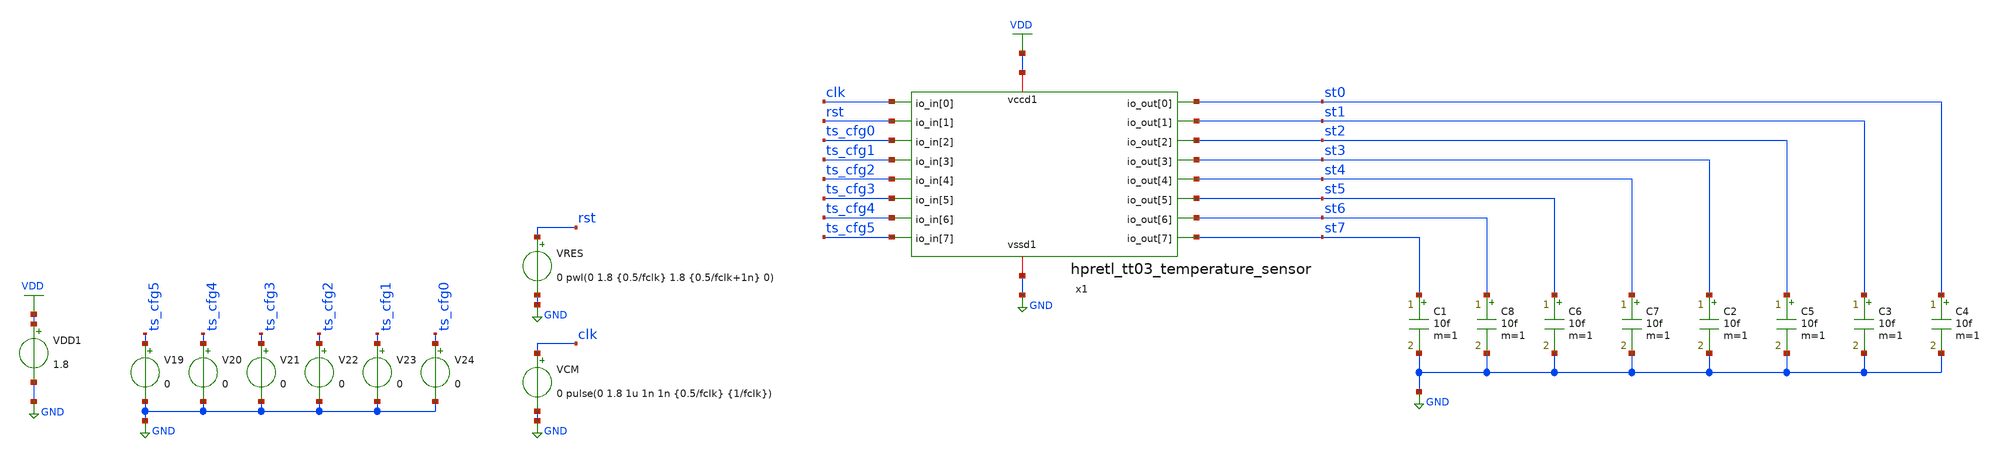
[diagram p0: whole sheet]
** sch_path: sim/tb_tempsens.sch
**.subckt tb_tempsens
VDD1 VDD GND 1.8
V19 ts_cfg5 GND 0
V20 ts_cfg4 GND 0
V21 ts_cfg3 GND 0
V22 ts_cfg2 GND 0
V23 ts_cfg1 GND 0
V24 ts_cfg0 GND 0
VCM clk GND 0 pulse(0 1.8 1u 1n 1n {0.5/fclk} {1/fclk})
VRES rst GND 0 pwl(0 1.8 {0.5/fclk} 1.8 {0.5/fclk+1n} 0)
x1 rst ts_cfg0 ts_cfg1 ts_cfg2 ts_cfg3 ts_cfg4 ts_cfg5 st0 st1 st2 st3 st4 st5 st6 st7 clk VDD GND
+ hpretl_tt03_temperature_sensor
C1 st7 GND 10f m=1
C3 st1 GND 10f m=1
C4 st0 GND 10f m=1
C2 st3 GND 10f m=1
C5 st2 GND 10f m=1
C6 st5 GND 10f m=1
C7 st4 GND 10f m=1
C8 st6 GND 10f m=1
**** begin user architecture code

** opencircuitdesign pdks install
.lib $::SKYWATER_MODELS/sky130.lib.spice tt





* ngspice commands
****************
.include ../hpretl_tt03_temperature_sensor.pex.spice
*.include /foss/pdk/sky130A/libs.ref/sky130_fd_sc_hd/spice/sky130_fd_sc_hd.spice

****************
* Misc
****************
.param fclk=10k
.options method=gear maxord=2
.temp 30

*.save all
.save clk rst st0 st1 st2 st3 st4 st5 st6 st7 i(VDD1)
.control
set num_threads=6
tran 10u 0.6

plot clk rst st0 st1 st2 st3 st4 st5 st6 st7

set wr_vecnames
write tb_tempsens.raw clk rst st0 st1 st2 st3 st4 st5 st6 st7 i(VDD1)
.endc



**** end user architecture code
**.ends
.GLOBAL VDD
.GLOBAL GND
.end
